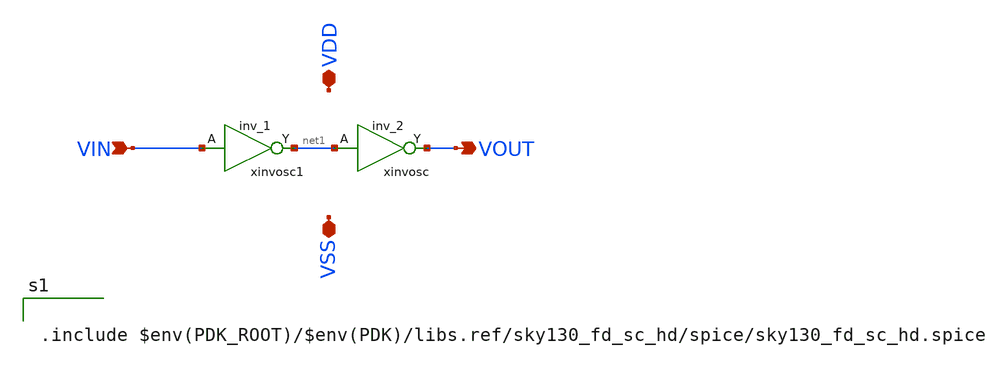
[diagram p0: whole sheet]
** sch_path: modules/BUFFMIN/symbol/BUFFMIN.sch
**.subckt BUFFMIN VDD VSS VIN VOUT
*.iopin VDD
*.iopin VSS
*.ipin VIN
*.opin VOUT
xinvosc net1 VSS VSS VDD VDD VOUT sky130_fd_sc_hd__inv_2
xinvosc1 VIN VSS VSS VDD VDD net1 sky130_fd_sc_hd__inv_1
**** begin user architecture code

.include $env(PDK_ROOT)/$env(PDK)/libs.ref/sky130_fd_sc_hd/spice/sky130_fd_sc_hd.spice

**** end user architecture code
**.ends
.end
